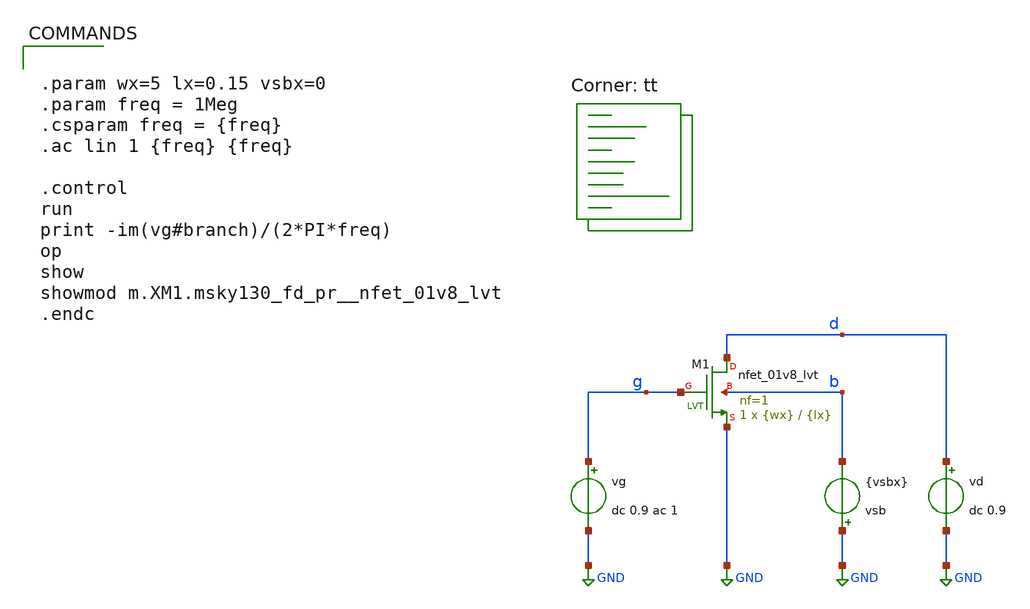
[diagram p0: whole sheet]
** sch_path: captest_nfet_01v8_lvt.sch
**.subckt captest_nfet_01v8_lvt
vg g GND dc 0.9 ac 1
vd d GND dc 0.9
vsb GND b {vsbx}
XM1 d g GND b sky130_fd_pr__nfet_01v8_lvt L={lx} W={wx} nf=1 ad='int((nf+1)/2) * W/nf * 0.29' as='int((nf+2)/2) * W/nf * 0.29'
+ pd='2*int((nf+1)/2) * (W/nf + 0.29)' ps='2*int((nf+2)/2) * (W/nf + 0.29)' nrd='0.29 / W' nrs='0.29 / W'
+ sa=0 sb=0 sd=0 mult=1 m=1
**** begin user architecture code


.param wx=5 lx=0.15 vsbx=0
.param freq = 1Meg
.csparam freq = {freq}
.ac lin 1 {freq} {freq}

.control
run
print -im(vg#branch)/(2*PI*freq)
op
show
showmod m.XM1.msky130_fd_pr__nfet_01v8_lvt
.endc


.lib $::SKYWATER_MODELS/sky130.lib.spice tt
**** end user architecture code
**.ends
.GLOBAL GND
.end
